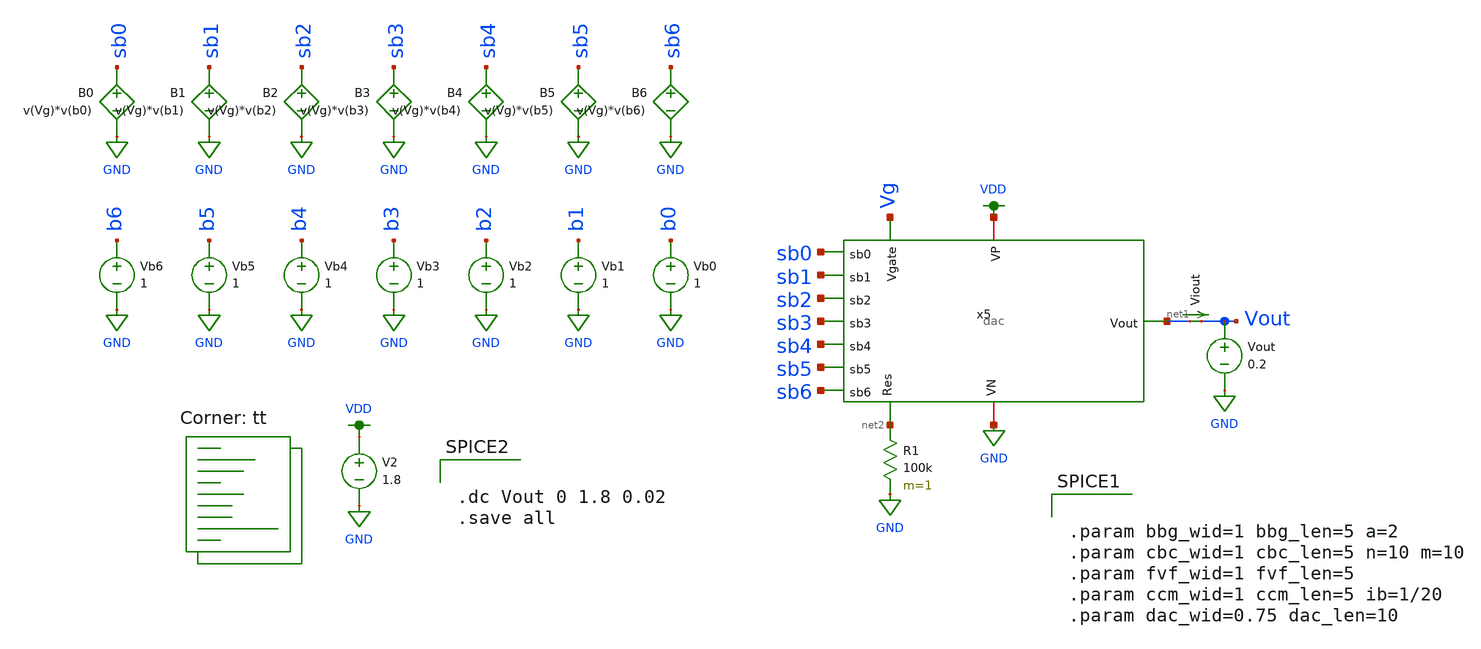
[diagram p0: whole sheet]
** sch_path: test_dac_vout.sch
**.subckt test_dac_vout
V2 VDD GND 1.8
R1 net2 GND 100k m=1
Vout Vout GND 0.2
Viout net1 Vout 0
.save i(viout)
Vb0 b0 GND 1
B0 sb0 GND V=v(Vg)*v(b0)
Vb1 b1 GND 1
B1 sb1 GND V=v(Vg)*v(b1)
Vb2 b2 GND 1
B2 sb2 GND V=v(Vg)*v(b2)
Vb3 b3 GND 1
B3 sb3 GND V=v(Vg)*v(b3)
Vb4 b4 GND 1
B4 sb4 GND V=v(Vg)*v(b4)
Vb5 b5 GND 1
B5 sb5 GND V=v(Vg)*v(b5)
Vb6 b6 GND 1
B6 sb6 GND V=v(Vg)*v(b6)
x5 VDD sb0 sb1 GND sb2 net1 Vg sb3 sb4 sb5 sb6 net2 dac
**** begin user architecture code
.lib $::SKYWATER_MODELS/sky130.lib.spice tt


.dc Vout 0 1.8 0.02
.save all




.param bbg_wid=1 bbg_len=5 a=2
.param cbc_wid=1 cbc_len=5 n=10 m=10
.param fvf_wid=1 fvf_len=5
.param ccm_wid=1 ccm_len=5 ib=1/20
.param dac_wid=0.75 dac_len=10


**** end user architecture code
**.ends
.GLOBAL GND
.GLOBAL VDD
.end
